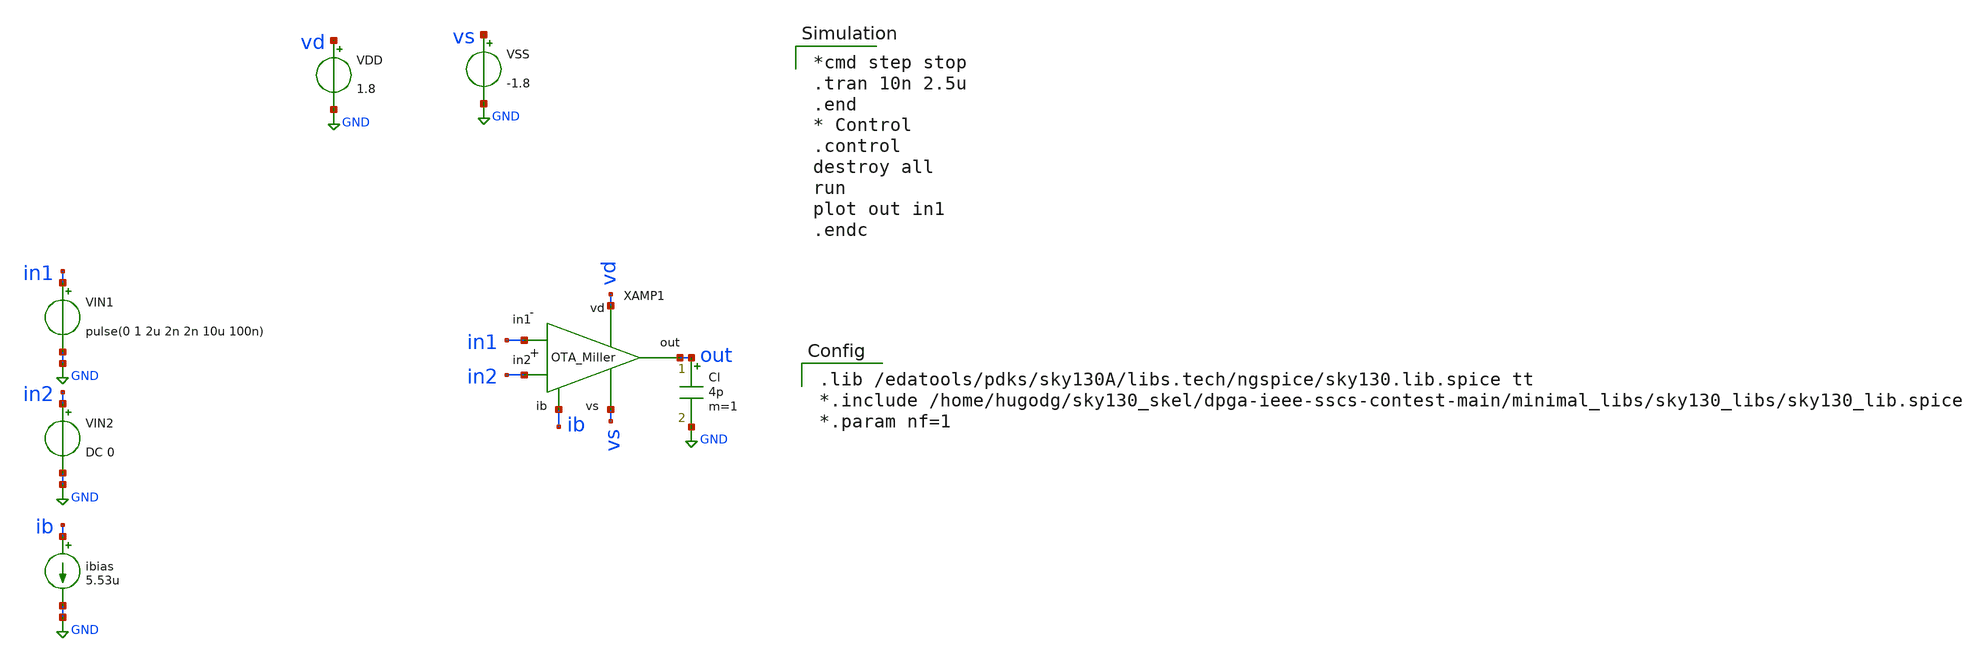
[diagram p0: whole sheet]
** sch_path: xschem/ota_tb-largesignal.sch
* Copyright 2020 Stefan Frederik Schippers
* Licensed under the Apache License, Version 2.0 (the "License");
* you may not use this file except in compliance with the License.
* You may obtain a copy of the License at
* https://www.apache.org/licenses/LICENSE-2.0
* Unless required by applicable law or agreed to in writing, software
* distributed under the License is distributed on an "AS IS" BASIS,
* WITHOUT WARRANTIES OR CONDITIONS OF ANY KIND, either express or implied.
* See the License for the specific language governing permissions and
* limitations under the License.
**.subckt ota_tb-largesignal
VIN2 in2 GND DC 0
VIN1 in1 GND pulse(0 1 2u 2n 2n 10u 100n)
ibias ib GND 5.53u
VDD vd GND 1.8
VSS vs GND -1.8
X1 vd ib out in2 in1 vs ota
Cl out GND 4p m=1
**** begin user architecture code

*cmd step stop
.tran 10n 2.5u
.end
* Control
.control
destroy all
run
plot out in1
.endc


.lib /edatools/pdks/sky130A/libs.tech/ngspice/sky130.lib.spice tt
*.include /home/hugodg/sky130_skel/dpga-ieee-sscs-contest-main/minimal_libs/sky130_libs/sky130_lib.spice
*.param nf=1

**** end user architecture code
**.ends

* expanding   symbol:  /home/hugodg/sky130_skel/dpga-ieee-sscs-contest-main/xschem/ota.sym # of
*+ pins=6
** sym_path: xschem/ota.sym
** sch_path: xschem/ota.sch
.subckt ota vd ib out in2 in1 vs
*.iopin vd
*.iopin vs
*.iopin ib
*.ipin in1
*.ipin in2
*.opin out
XM4 d c vs vs sky130_fd_pr__nfet_01v8 L=1 W=0.861 nf=1 ad='int((nf+1)/2) * W/nf * 0.29' as='int((nf+2)/2) * W/nf * 0.29'
+ pd='2*int((nf+1)/2) * (W/nf + 0.29)' ps='2*int((nf+2)/2) * (W/nf + 0.29)' nrd='0.29 / W' nrs='0.29 / W'
+ sa=0 sb=0 sd=0 mult=1 m=1
XM7 e d vs vs sky130_fd_pr__nfet_01v8 L=1 W=8.61 nf=2 ad='int((nf+1)/2) * W/nf * 0.29' as='int((nf+2)/2) * W/nf * 0.29'
+ pd='2*int((nf+1)/2) * (W/nf + 0.29)' ps='2*int((nf+2)/2) * (W/nf + 0.29)' nrd='0.29 / W' nrs='0.29 / W'
+ sa=0 sb=0 sd=0 mult=1 m=1
XM5 ib ib vd vd sky130_fd_pr__pfet_01v8 L=1 W=5.85 nf=1 ad='int((nf+1)/2) * W/nf * 0.29' as='int((nf+2)/2) * W/nf * 0.29'
+ pd='2*int((nf+1)/2) * (W/nf + 0.29)' ps='2*int((nf+2)/2) * (W/nf + 0.29)' nrd='0.29 / W' nrs='0.29 / W'
+ sa=0 sb=0 sd=0 mult=1 m=1
XM6 b ib vd vd sky130_fd_pr__pfet_01v8 L=1 W=5.85 nf=1 ad='int((nf+1)/2) * W/nf * 0.29' as='int((nf+2)/2) * W/nf * 0.29'
+ pd='2*int((nf+1)/2) * (W/nf + 0.29)' ps='2*int((nf+2)/2) * (W/nf + 0.29)' nrd='0.29 / W' nrs='0.29 / W'
+ sa=0 sb=0 sd=0 mult=1 m=1
XM8 e ib vd vd sky130_fd_pr__pfet_01v8 L=1 W=29.3 nf=5 ad='int((nf+1)/2) * W/nf * 0.29' as='int((nf+2)/2) * W/nf * 0.29'
+ pd='2*int((nf+1)/2) * (W/nf + 0.29)' ps='2*int((nf+2)/2) * (W/nf + 0.29)' nrd='0.29 / W' nrs='0.29 / W'
+ sa=0 sb=0 sd=0 mult=1 m=1
XM10 out ib vd vd sky130_fd_pr__pfet_01v8 L=1 W=5.85 nf=1 ad='int((nf+1)/2) * W/nf * 0.29' as='int((nf+2)/2) * W/nf * 0.29'
+ pd='2*int((nf+1)/2) * (W/nf + 0.29)' ps='2*int((nf+2)/2) * (W/nf + 0.29)' nrd='0.29 / W' nrs='0.29 / W'
+ sa=0 sb=0 sd=0 mult=1 m=1
XM9 vs e out out sky130_fd_pr__pfet_01v8 L=1 W=5.85 nf=1 ad='int((nf+1)/2) * W/nf * 0.29' as='int((nf+2)/2) * W/nf * 0.29'
+ pd='2*int((nf+1)/2) * (W/nf + 0.29)' ps='2*int((nf+2)/2) * (W/nf + 0.29)' nrd='0.29 / W' nrs='0.29 / W'
+ sa=0 sb=0 sd=0 mult=1 m=1
XM1 c in1 b b sky130_fd_pr__pfet_01v8 L=1 W=2.93 nf=1 ad='int((nf+1)/2) * W/nf * 0.29' as='int((nf+2)/2) * W/nf * 0.29'
+ pd='2*int((nf+1)/2) * (W/nf + 0.29)' ps='2*int((nf+2)/2) * (W/nf + 0.29)' nrd='0.29 / W' nrs='0.29 / W'
+ sa=0 sb=0 sd=0 mult=1 m=1
XM2 d in2 b b sky130_fd_pr__pfet_01v8 L=1 W=2.93 nf=1 ad='int((nf+1)/2) * W/nf * 0.29' as='int((nf+2)/2) * W/nf * 0.29'
+ pd='2*int((nf+1)/2) * (W/nf + 0.29)' ps='2*int((nf+2)/2) * (W/nf + 0.29)' nrd='0.29 / W' nrs='0.29 / W'
+ sa=0 sb=0 sd=0 mult=1 m=1
XM3 c c vs vs sky130_fd_pr__nfet_01v8 L=1 W=0.861 nf=1 ad='int((nf+1)/2) * W/nf * 0.29' as='int((nf+2)/2) * W/nf * 0.29'
+ pd='2*int((nf+1)/2) * (W/nf + 0.29)' ps='2*int((nf+2)/2) * (W/nf + 0.29)' nrd='0.29 / W' nrs='0.29 / W'
+ sa=0 sb=0 sd=0 mult=1 m=1
XCC e d sky130_fd_pr__cap_mim_m3_1 W=22.023 L=22.023 MF=1 m=1
.ends

.GLOBAL GND
.end
